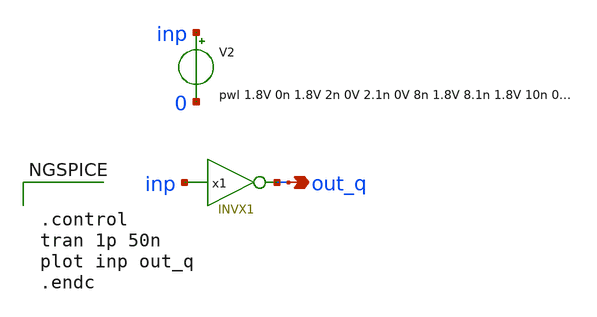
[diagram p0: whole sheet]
** sch_path: sky130A/libs.tech/xschem/test_INVX1.sch
**.subckt test_INVX1 out_q
*.opin out_q
V2 inp 0
pwl 1.8V 0n 1.8V 2n 0V 2.1n 0V 8n 1.8V 8.1n 1.8V 10n 0V 10.1n 0V 13.9n 1.8V 14n

x1 inp out_q INVX1 VDD VSS INVX1
**** begin user architecture code


.control
tran 1p 50n
plot inp out_q
.endc




.lib $::SKYWATER_MODELS/sky130.lib.spice tt



**** end user architecture code
**.ends

* expanding   symbol:  INVX1.sym # of pins=2
** sym_path: sky130A/libs.tech/xschem/sky130_tests/INVX1.sym
** sch_path: sky130A/libs.tech/xschem/sky130_tests/INVX1.sch
.subckt INVX1 A Y
*.ipin A
*.opin Y
XM1 Y A VSSPIN VSSPIN sky130_fd_pr__nfet_01v8 L=0.15 W=3 nf=1 ad='int((nf+1)/2) * W/nf * 0.29' as='int((nf+2)/2) * W/nf * 0.29'
+ pd='2*int((nf+1)/2) * (W/nf + 0.29)' ps='2*int((nf+2)/2) * (W/nf + 0.29)' nrd='0.29 / W' nrs='0.29 / W'
+ sa=0 sb=0 sd=0 mult=1 m=1
XM2 Y A VDDPIN VDDPIN sky130_fd_pr__pfet_01v8 L=0.15 W=2 nf=1 ad='int((nf+1)/2) * W/nf * 0.29' as='int((nf+2)/2) * W/nf * 0.29'
+ pd='2*int((nf+1)/2) * (W/nf + 0.29)' ps='2*int((nf+2)/2) * (W/nf + 0.29)' nrd='0.29 / W' nrs='0.29 / W'
+ sa=0 sb=0 sd=0 mult=1 m=1
XM3 Y A VDDPIN VDDPIN sky130_fd_pr__pfet_01v8 L=0.15 W=2 nf=1 ad='int((nf+1)/2) * W/nf * 0.29' as='int((nf+2)/2) * W/nf * 0.29'
+ pd='2*int((nf+1)/2) * (W/nf + 0.29)' ps='2*int((nf+2)/2) * (W/nf + 0.29)' nrd='0.29 / W' nrs='0.29 / W'
+ sa=0 sb=0 sd=0 mult=1 m=1
.ends

.end
